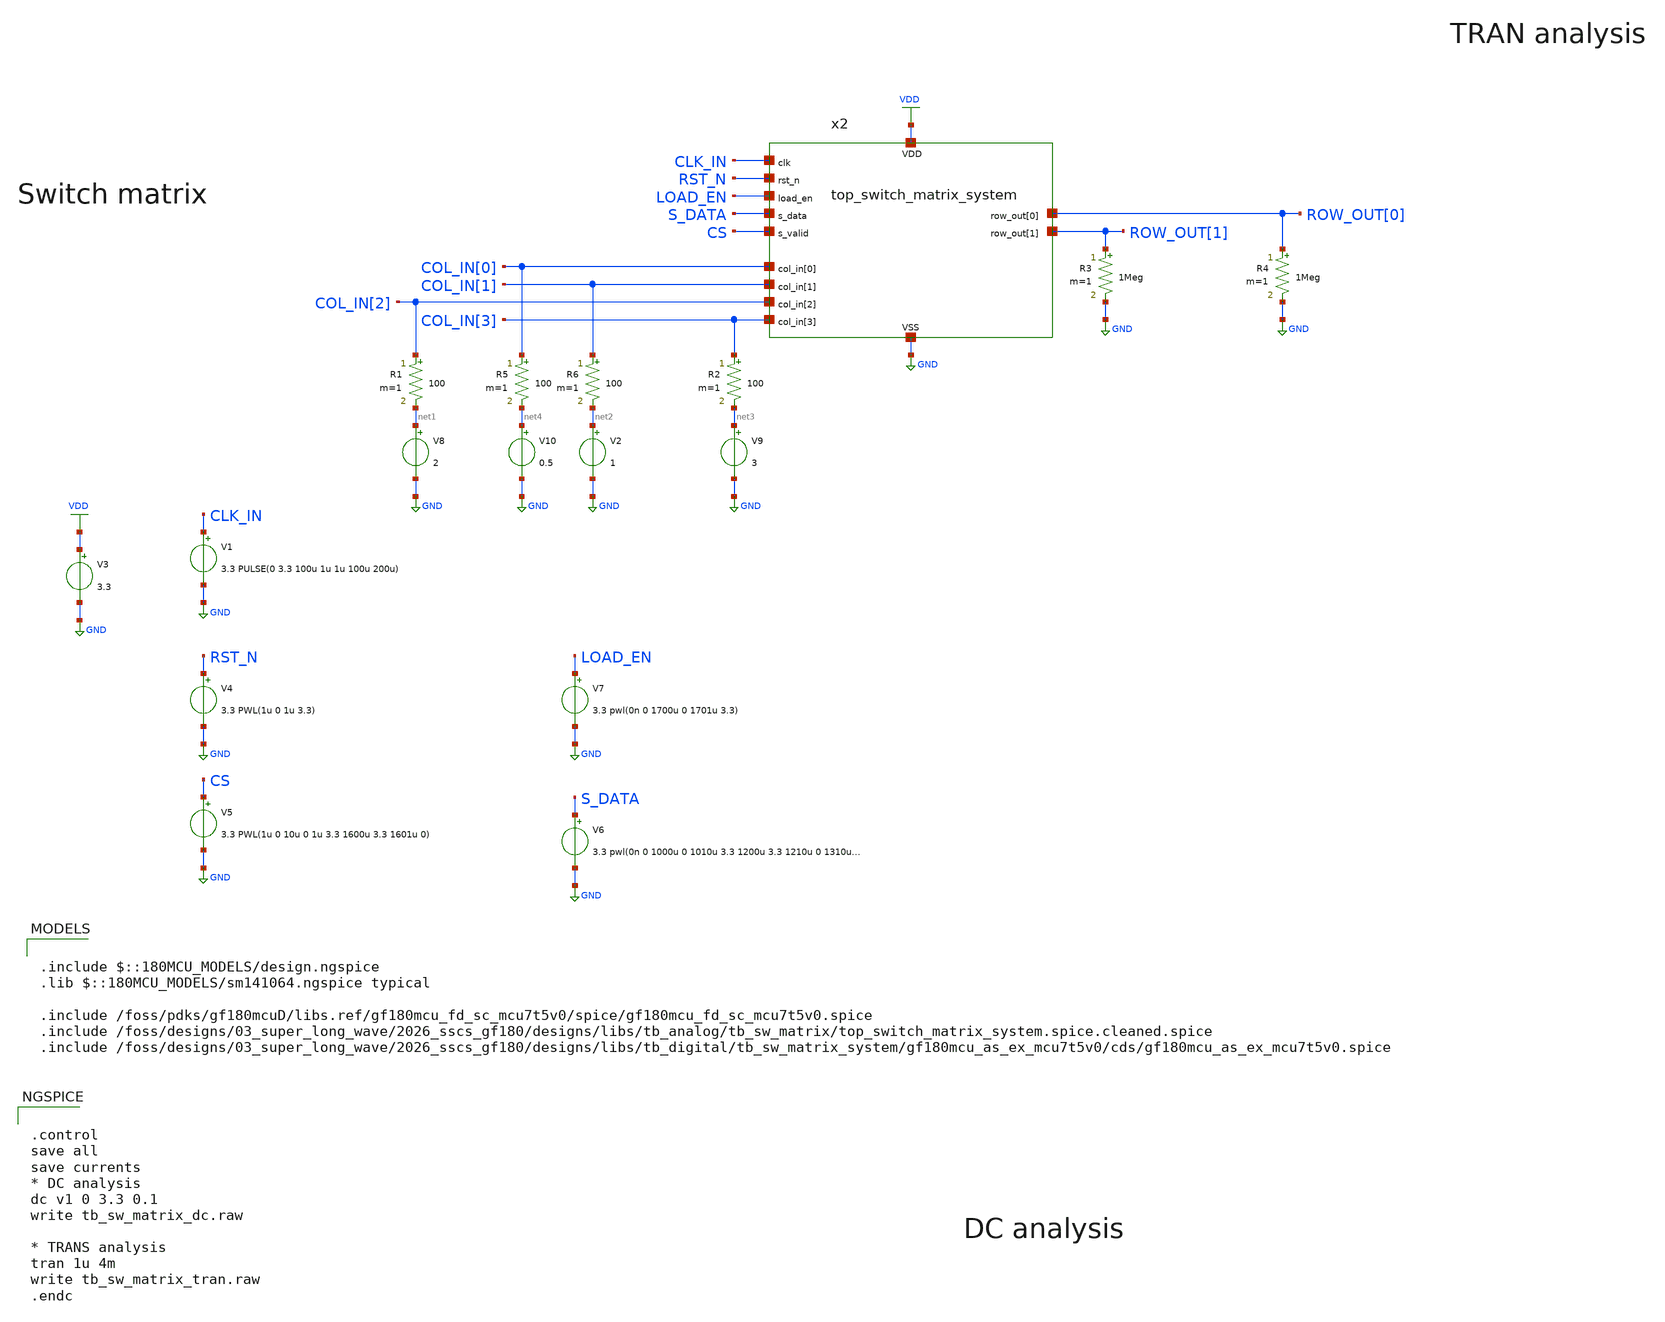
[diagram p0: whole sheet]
** sch_path: designs/libs/tb_analog/tb_sw_matrix/tb_sw_matrix.sch
* Copyright 2022 GlobalFoundries PDK Authors
* Licensed under the Apache License, Version 2.0 (the "License");
* you may not use this file except in compliance with the License.
* You may obtain a copy of the License at
* https://www.apache.org/licenses/LICENSE-2.0
* Unless required by applicable law or agreed to in writing, software
* distributed under the License is distributed on an "AS IS" BASIS,
* WITHOUT WARRANTIES OR CONDITIONS OF ANY KIND, either express or implied.
* See the License for the specific language governing permissions and
* limitations under the License.
**.subckt tb_sw_matrix
V1 CLK_IN GND 3.3 PULSE(0 3.3 100u 1u 1u 100u 200u)
V3 VDD GND 3.3
x2 VDD GND CLK_IN COL_IN[0] COL_IN[1] COL_IN[2] COL_IN[3] LOAD_EN ROW_OUT[0] ROW_OUT[1] RST_N S_DATA
+ CS top_switch_matrix_system
R3 ROW_OUT[1] GND 1Meg m=1
R4 ROW_OUT[0] GND 1Meg m=1
V4 RST_N GND 3.3 PWL(1u 0 1u 3.3)
V5 CS GND 3.3 PWL(1u 0 10u 0 1u 3.3 1600u 3.3 1601u 0)
V6 S_DATA GND 3.3 pwl(0n 0 1000u 0 1010u 3.3 1200u 3.3 1210u 0 1310u 0)
V7 LOAD_EN GND 3.3 pwl(0n 0 1700u 0 1701u 3.3)
R1 COL_IN[2] net1 100 m=1
R6 COL_IN[1] net2 100 m=1
V2 net2 GND 1
V8 net1 GND 2
R2 COL_IN[3] net3 100 m=1
V9 net3 GND 3
R5 COL_IN[0] net4 100 m=1
V10 net4 GND 0.5
**** begin user architecture code

.include $::180MCU_MODELS/design.ngspice
.lib $::180MCU_MODELS/sm141064.ngspice typical

.include /foss/pdks/gf180mcuD/libs.ref/gf180mcu_fd_sc_mcu7t5v0/spice/gf180mcu_fd_sc_mcu7t5v0.spice
.include /foss/designs/03_super_long_wave/2026_sscs_gf180/designs/libs/tb_analog/tb_sw_matrix/top_switch_matrix_system.spice.cleaned.spice
.include /foss/designs/03_super_long_wave/2026_sscs_gf180/designs/libs/tb_digital/tb_sw_matrix_system/gf180mcu_as_ex_mcu7t5v0/cds/gf180mcu_as_ex_mcu7t5v0.spice



.control
save all
save currents
* DC analysis
dc v1 0 3.3 0.1
write tb_sw_matrix_dc.raw

* TRANS analysis
tran 1u 4m
write tb_sw_matrix_tran.raw
.endc


**** end user architecture code
**.ends
.GLOBAL GND
.GLOBAL VDD
.end
